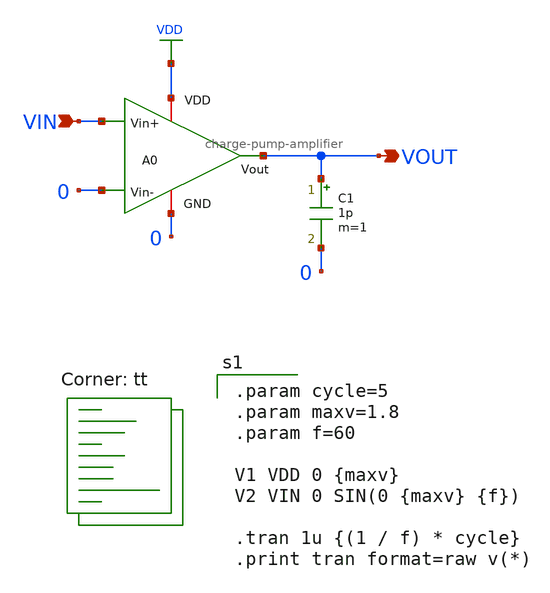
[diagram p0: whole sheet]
** sch_path: charge-pump/charge-pump-amplifier-test.sch
**.subckt charge-pump-amplifier-test VOUT VIN
*.opin VOUT
*.ipin VIN
A0 VDD VOUT VIN 0 0 charge-pump-amplifier
C1 VOUT 0 1p m=1
**** begin user architecture code
.lib $::SKYWATER_MODELS/sky130.lib.spice tt

.param cycle=5
.param maxv=1.8
.param f=60

V1 VDD 0 {maxv}
V2 VIN 0 SIN(0 {maxv} {f})

.tran 1u {(1 / f) * cycle}
.print tran format=raw v(*)


**** end user architecture code
**.ends

* expanding   symbol:  charge-pump-amplifier.sym # of pins=5
** sym_path: charge-pump/charge-pump-amplifier.sym
** sch_path: charge-pump/charge-pump-amplifier.sch
.subckt charge-pump-amplifier VDD Vout Vin+ Vin- GND
*.ipin Vin+
*.ipin Vin-
*.opin Vout
*.iopin VDD
*.iopin GND
XM1p net8 net4 net1 net1 sky130_fd_pr__pfet_01v8 L=0.15 W=1 nf=1 ad='int((nf+1)/2) * W/nf * 0.29' as='int((nf+2)/2) * W/nf * 0.29'
+ pd='2*int((nf+1)/2) * (W/nf + 0.29)' ps='2*int((nf+2)/2) * (W/nf + 0.29)' nrd='0.29 / W' nrs='0.29 / W'
+ sa=0 sb=0 sd=0 mult=1 m=1
XM1n net7 Vin+ net2 net2 sky130_fd_pr__nfet_01v8 L=0.15 W=1 nf=1 ad='int((nf+1)/2) * W/nf * 0.29' as='int((nf+2)/2) * W/nf * 0.29'
+ pd='2*int((nf+1)/2) * (W/nf + 0.29)' ps='2*int((nf+2)/2) * (W/nf + 0.29)' nrd='0.29 / W' nrs='0.29 / W'
+ sa=0 sb=0 sd=0 mult=1 m=1
XM2n net6 Vin- net2 net2 sky130_fd_pr__nfet_01v8 L=0.15 W=1 nf=1 ad='int((nf+1)/2) * W/nf * 0.29' as='int((nf+2)/2) * W/nf * 0.29'
+ pd='2*int((nf+1)/2) * (W/nf + 0.29)' ps='2*int((nf+2)/2) * (W/nf + 0.29)' nrd='0.29 / W' nrs='0.29 / W'
+ sa=0 sb=0 sd=0 mult=1 m=1
XM2p net9 net5 net1 net1 sky130_fd_pr__pfet_01v8 L=0.15 W=1 nf=1 ad='int((nf+1)/2) * W/nf * 0.29' as='int((nf+2)/2) * W/nf * 0.29'
+ pd='2*int((nf+1)/2) * (W/nf + 0.29)' ps='2*int((nf+2)/2) * (W/nf + 0.29)' nrd='0.29 / W' nrs='0.29 / W'
+ sa=0 sb=0 sd=0 mult=1 m=1
XM3 net3 net3 VDD VDD sky130_fd_pr__pfet_01v8 L=0.15 W=1 nf=1 ad='int((nf+1)/2) * W/nf * 0.29' as='int((nf+2)/2) * W/nf * 0.29'
+ pd='2*int((nf+1)/2) * (W/nf + 0.29)' ps='2*int((nf+2)/2) * (W/nf + 0.29)' nrd='0.29 / W' nrs='0.29 / W'
+ sa=0 sb=0 sd=0 mult=1 m=1
XM4 VDD Vin+ net4 net4 sky130_fd_pr__nfet_01v8 L=0.15 W=1 nf=1 ad='int((nf+1)/2) * W/nf * 0.29' as='int((nf+2)/2) * W/nf * 0.29'
+ pd='2*int((nf+1)/2) * (W/nf + 0.29)' ps='2*int((nf+2)/2) * (W/nf + 0.29)' nrd='0.29 / W' nrs='0.29 / W'
+ sa=0 sb=0 sd=0 mult=1 m=1
XM5 net1 net3 VDD VDD sky130_fd_pr__pfet_01v8 L=0.15 W=1 nf=1 ad='int((nf+1)/2) * W/nf * 0.29' as='int((nf+2)/2) * W/nf * 0.29'
+ pd='2*int((nf+1)/2) * (W/nf + 0.29)' ps='2*int((nf+2)/2) * (W/nf + 0.29)' nrd='0.29 / W' nrs='0.29 / W'
+ sa=0 sb=0 sd=0 mult=1 m=1
XM6 net7 net7 VDD VDD sky130_fd_pr__pfet_01v8 L=0.15 W=1 nf=1 ad='int((nf+1)/2) * W/nf * 0.29' as='int((nf+2)/2) * W/nf * 0.29'
+ pd='2*int((nf+1)/2) * (W/nf + 0.29)' ps='2*int((nf+2)/2) * (W/nf + 0.29)' nrd='0.29 / W' nrs='0.29 / W'
+ sa=0 sb=0 sd=0 mult=1 m=1
XM7 net6 net6 VDD VDD sky130_fd_pr__pfet_01v8 L=0.15 W=1 nf=1 ad='int((nf+1)/2) * W/nf * 0.29' as='int((nf+2)/2) * W/nf * 0.29'
+ pd='2*int((nf+1)/2) * (W/nf + 0.29)' ps='2*int((nf+2)/2) * (W/nf + 0.29)' nrd='0.29 / W' nrs='0.29 / W'
+ sa=0 sb=0 sd=0 mult=1 m=1
XM8 VDD Vin- net5 net5 sky130_fd_pr__nfet_01v8 L=0.15 W=1 nf=1 ad='int((nf+1)/2) * W/nf * 0.29' as='int((nf+2)/2) * W/nf * 0.29'
+ pd='2*int((nf+1)/2) * (W/nf + 0.29)' ps='2*int((nf+2)/2) * (W/nf + 0.29)' nrd='0.29 / W' nrs='0.29 / W'
+ sa=0 sb=0 sd=0 mult=1 m=1
XM9 net9 net7 VDD VDD sky130_fd_pr__pfet_01v8 L=0.15 W=1 nf=1 ad='int((nf+1)/2) * W/nf * 0.29' as='int((nf+2)/2) * W/nf * 0.29'
+ pd='2*int((nf+1)/2) * (W/nf + 0.29)' ps='2*int((nf+2)/2) * (W/nf + 0.29)' nrd='0.29 / W' nrs='0.29 / W'
+ sa=0 sb=0 sd=0 mult=1 m=1
XM10 net8 net6 VDD VDD sky130_fd_pr__pfet_01v8 L=0.15 W=1 nf=1 ad='int((nf+1)/2) * W/nf * 0.29' as='int((nf+2)/2) * W/nf * 0.29'
+ pd='2*int((nf+1)/2) * (W/nf + 0.29)' ps='2*int((nf+2)/2) * (W/nf + 0.29)' nrd='0.29 / W' nrs='0.29 / W'
+ sa=0 sb=0 sd=0 mult=1 m=1
XM11 net10 net3 VDD VDD sky130_fd_pr__pfet_01v8 L=0.15 W=1 nf=1 ad='int((nf+1)/2) * W/nf * 0.29' as='int((nf+2)/2) * W/nf * 0.29'
+ pd='2*int((nf+1)/2) * (W/nf + 0.29)' ps='2*int((nf+2)/2) * (W/nf + 0.29)' nrd='0.29 / W' nrs='0.29 / W'
+ sa=0 sb=0 sd=0 mult=1 m=1
XM12 net11 net3 VDD VDD sky130_fd_pr__pfet_01v8 L=0.15 W=1 nf=1 ad='int((nf+1)/2) * W/nf * 0.29' as='int((nf+2)/2) * W/nf * 0.29'
+ pd='2*int((nf+1)/2) * (W/nf + 0.29)' ps='2*int((nf+2)/2) * (W/nf + 0.29)' nrd='0.29 / W' nrs='0.29 / W'
+ sa=0 sb=0 sd=0 mult=1 m=1
XM13 net10 VDD net9 net9 sky130_fd_pr__nfet_01v8 L=0.15 W=1 nf=1 ad='int((nf+1)/2) * W/nf * 0.29' as='int((nf+2)/2) * W/nf * 0.29'
+ pd='2*int((nf+1)/2) * (W/nf + 0.29)' ps='2*int((nf+2)/2) * (W/nf + 0.29)' nrd='0.29 / W' nrs='0.29 / W'
+ sa=0 sb=0 sd=0 mult=1 m=1
XM14 net11 VDD net8 net8 sky130_fd_pr__nfet_01v8 L=0.15 W=1 nf=1 ad='int((nf+1)/2) * W/nf * 0.29' as='int((nf+2)/2) * W/nf * 0.29'
+ pd='2*int((nf+1)/2) * (W/nf + 0.29)' ps='2*int((nf+2)/2) * (W/nf + 0.29)' nrd='0.29 / W' nrs='0.29 / W'
+ sa=0 sb=0 sd=0 mult=1 m=1
XM15 Vout net3 VDD VDD sky130_fd_pr__pfet_01v8 L=0.15 W=1 nf=1 ad='int((nf+1)/2) * W/nf * 0.29' as='int((nf+2)/2) * W/nf * 0.29'
+ pd='2*int((nf+1)/2) * (W/nf + 0.29)' ps='2*int((nf+2)/2) * (W/nf + 0.29)' nrd='0.29 / W' nrs='0.29 / W'
+ sa=0 sb=0 sd=0 mult=1 m=1
XM16 net10 net10 GND GND sky130_fd_pr__nfet_01v8 L=0.15 W=1 nf=1 ad='int((nf+1)/2) * W/nf * 0.29' as='int((nf+2)/2) * W/nf * 0.29'
+ pd='2*int((nf+1)/2) * (W/nf + 0.29)' ps='2*int((nf+2)/2) * (W/nf + 0.29)' nrd='0.29 / W' nrs='0.29 / W'
+ sa=0 sb=0 sd=0 mult=1 m=1
XM17 net4 net10 GND GND sky130_fd_pr__nfet_01v8 L=0.15 W=1 nf=1 ad='int((nf+1)/2) * W/nf * 0.29' as='int((nf+2)/2) * W/nf * 0.29'
+ pd='2*int((nf+1)/2) * (W/nf + 0.29)' ps='2*int((nf+2)/2) * (W/nf + 0.29)' nrd='0.29 / W' nrs='0.29 / W'
+ sa=0 sb=0 sd=0 mult=1 m=1
XM18 net2 net10 GND GND sky130_fd_pr__nfet_01v8 L=0.15 W=1 nf=1 ad='int((nf+1)/2) * W/nf * 0.29' as='int((nf+2)/2) * W/nf * 0.29'
+ pd='2*int((nf+1)/2) * (W/nf + 0.29)' ps='2*int((nf+2)/2) * (W/nf + 0.29)' nrd='0.29 / W' nrs='0.29 / W'
+ sa=0 sb=0 sd=0 mult=1 m=1
XM19 net5 net10 GND GND sky130_fd_pr__nfet_01v8 L=0.15 W=1 nf=1 ad='int((nf+1)/2) * W/nf * 0.29' as='int((nf+2)/2) * W/nf * 0.29'
+ pd='2*int((nf+1)/2) * (W/nf + 0.29)' ps='2*int((nf+2)/2) * (W/nf + 0.29)' nrd='0.29 / W' nrs='0.29 / W'
+ sa=0 sb=0 sd=0 mult=1 m=1
XM20 net9 net10 GND GND sky130_fd_pr__nfet_01v8 L=0.15 W=1 nf=1 ad='int((nf+1)/2) * W/nf * 0.29' as='int((nf+2)/2) * W/nf * 0.29'
+ pd='2*int((nf+1)/2) * (W/nf + 0.29)' ps='2*int((nf+2)/2) * (W/nf + 0.29)' nrd='0.29 / W' nrs='0.29 / W'
+ sa=0 sb=0 sd=0 mult=1 m=1
XM21 net8 net10 GND GND sky130_fd_pr__nfet_01v8 L=0.15 W=1 nf=1 ad='int((nf+1)/2) * W/nf * 0.29' as='int((nf+2)/2) * W/nf * 0.29'
+ pd='2*int((nf+1)/2) * (W/nf + 0.29)' ps='2*int((nf+2)/2) * (W/nf + 0.29)' nrd='0.29 / W' nrs='0.29 / W'
+ sa=0 sb=0 sd=0 mult=1 m=1
XM22 Vout net11 GND GND sky130_fd_pr__nfet_01v8 L=0.15 W=1 nf=1 ad='int((nf+1)/2) * W/nf * 0.29' as='int((nf+2)/2) * W/nf * 0.29'
+ pd='2*int((nf+1)/2) * (W/nf + 0.29)' ps='2*int((nf+2)/2) * (W/nf + 0.29)' nrd='0.29 / W' nrs='0.29 / W'
+ sa=0 sb=0 sd=0 mult=1 m=1
CL Vout GND 1p m=1
Cm net12 Vout 1p m=1
Rb1 net3 GND 500 m=1
Rb2 VDD net10 500 m=1
Rm net11 net12 500 m=1
.ends

.GLOBAL VDD
.end
